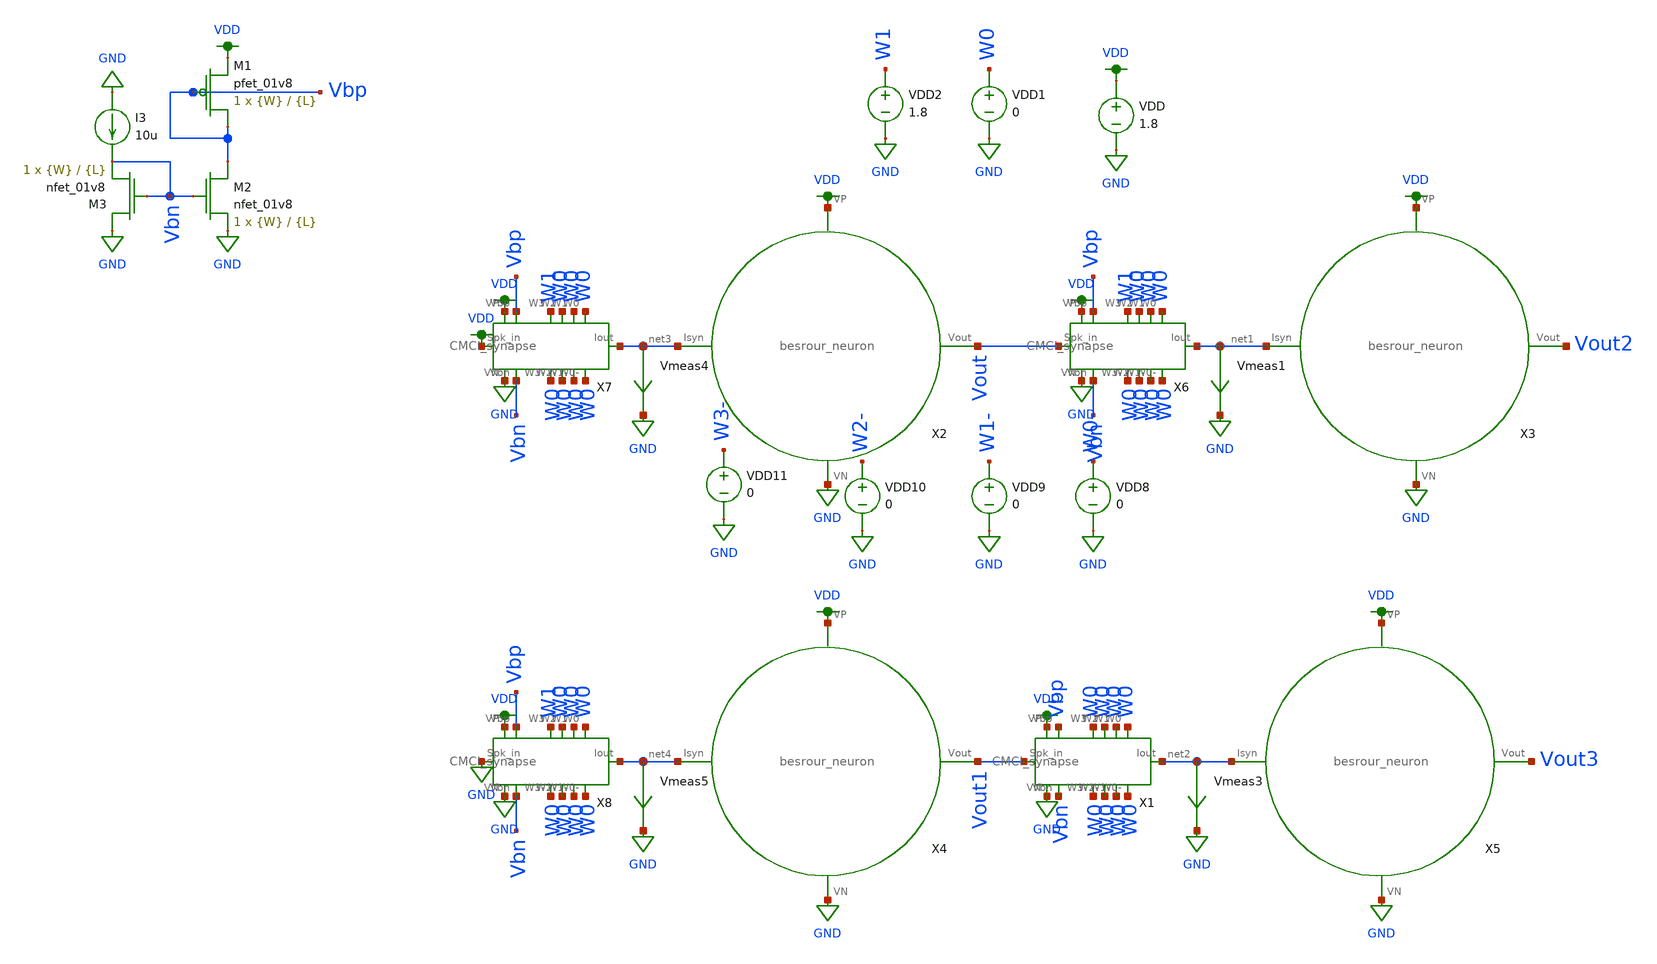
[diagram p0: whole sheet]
** sch_path: schematic/tran_besrour_CMCI.sch
**.subckt tran_besrour_CMCI
X2 net3 Vout VDD GND besrour_neuron
X4 net4 Vout1 VDD GND besrour_neuron
VDD VDD GND 1.8
VDD1 W0 GND 0
VDD2 W1 GND 1.8
Vmeas1 net1 GND 0
.save i(vmeas1)
XM1 Vbp Vbp VDD VDD sky130_fd_pr__pfet_01v8 L={L} W={W} nf=1 ad='int((nf+1)/2) * W/nf * 0.29' as='int((nf+2)/2) * W/nf * 0.29'
+ pd='2*int((nf+1)/2) * (W/nf + 0.29)' ps='2*int((nf+2)/2) * (W/nf + 0.29)' nrd='0.29 / W' nrs='0.29 / W'
+ sa=0 sb=0 sd=0 mult=1 m=1
XM2 Vbp Vbn GND GND sky130_fd_pr__nfet_01v8 L={L} W={W} nf=1 ad='int((nf+1)/2) * W/nf * 0.29' as='int((nf+2)/2) * W/nf * 0.29'
+ pd='2*int((nf+1)/2) * (W/nf + 0.29)' ps='2*int((nf+2)/2) * (W/nf + 0.29)' nrd='0.29 / W' nrs='0.29 / W'
+ sa=0 sb=0 sd=0 mult=1 m=1
XM3 GND Vbn Vbn GND sky130_fd_pr__nfet_01v8 L={L} W={W} nf=1 ad='int((nf+1)/2) * W/nf * 0.29' as='int((nf+2)/2) * W/nf * 0.29'
+ pd='2*int((nf+1)/2) * (W/nf + 0.29)' ps='2*int((nf+2)/2) * (W/nf + 0.29)' nrd='0.29 / W' nrs='0.29 / W'
+ sa=0 sb=0 sd=0 mult=1 m=1
I3 GND Vbn 10u
X3 net1 Vout2 VDD GND besrour_neuron
X5 net2 Vout3 VDD GND besrour_neuron
X6 VDD Vbp W1 W0 W0 W0 net1 W0 W0 W0 W0 Vbn GND Vout CMCI_synapse
X1 VDD Vbp W0 W0 W0 W0 net2 W0 W0 W0 W0 Vbn GND Vout1 CMCI_synapse
Vmeas3 net2 GND 0
.save i(vmeas3)
Vmeas4 net3 GND 0
.save i(vmeas4)
X7 VDD Vbp W1 W0 W0 W0 net3 W0 W0 W0 W0 Vbn GND VDD CMCI_synapse
Vmeas5 net4 GND 0
.save i(vmeas5)
X8 VDD Vbp W1 W0 W0 W0 net4 W0 W0 W0 W0 Vbn GND GND CMCI_synapse
VDD8 W0- GND 0
VDD9 W1- GND 0
VDD10 W2- GND 0
VDD11 W3- GND 0
**** begin user architecture code

.param W=1
.param L=0.15
.tran 0.1n 250n
.save all


.option wnflag=1
.param MC_SWITCH=0.0
.lib ~/skywater/skywater-pdk/libraries/sky130_fd_pr_ngspice/latest/models/sky130.lib.spice tt

**** end user architecture code
**.ends
.GLOBAL VDD
.GLOBAL GND
.end
